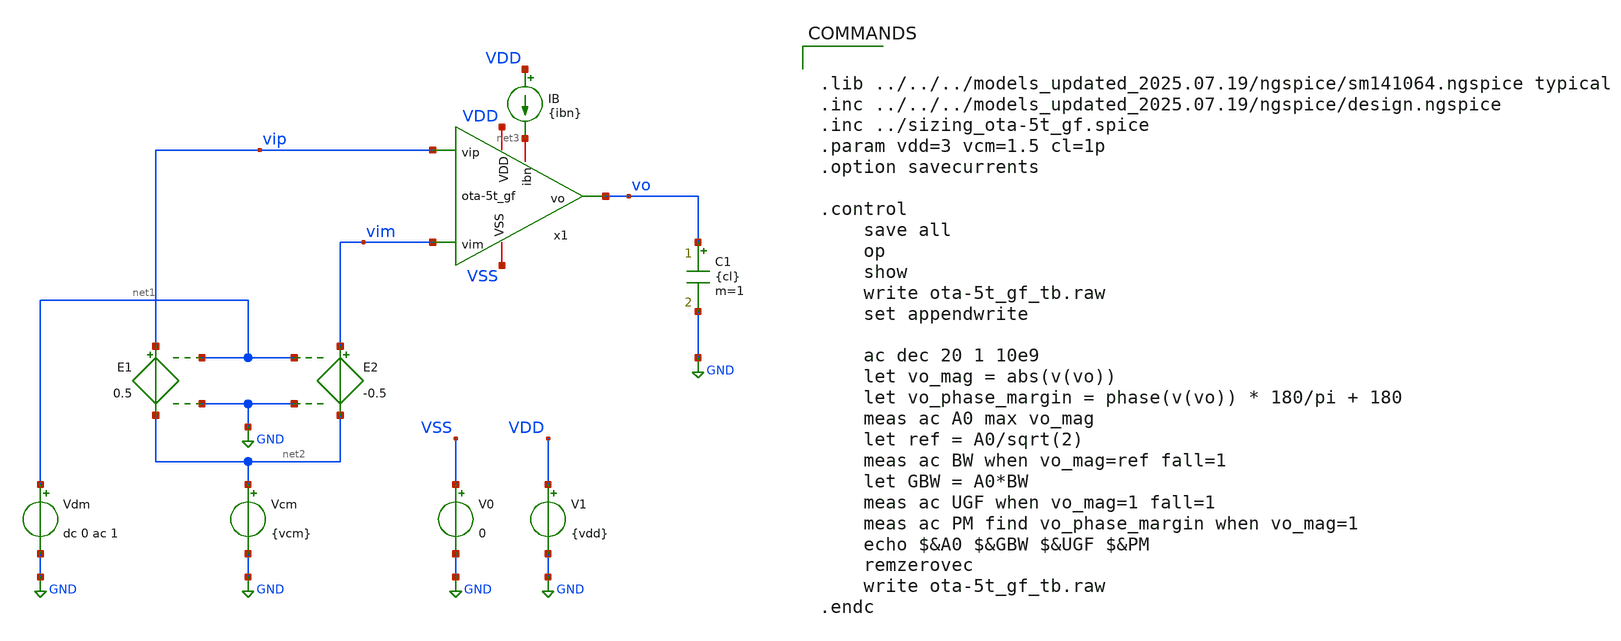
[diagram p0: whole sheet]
** sch_path: designs/libs/bmurmann_gmoverid/ota-5t/xschem/ota-5t_gf_tb.sch
**.subckt ota-5t_gf_tb
x1 vip vim vo VDD VSS net3 ota-5t_gf
E1 vip net2 net1 GND 0.5
E2 vim net2 net1 GND -0.5
Vdm net1 GND dc 0 ac 1
Vcm net2 GND {vcm}
V0 VSS GND 0
V1 VDD GND {vdd}
C1 vo GND {cl} m=1
IB VDD net3 {ibn}
**** begin user architecture code


.lib ../../../models_updated_2025.07.19/ngspice/sm141064.ngspice typical
.inc ../../../models_updated_2025.07.19/ngspice/design.ngspice
.inc ../sizing_ota-5t_gf.spice
.param vdd=3 vcm=1.5 cl=1p
.option savecurrents

.control
    save all
    op
    show
    write ota-5t_gf_tb.raw
    set appendwrite

    ac dec 20 1 10e9
    let vo_mag = abs(v(vo))
    let vo_phase_margin = phase(v(vo)) * 180/pi + 180
    meas ac A0 max vo_mag
    let ref = A0/sqrt(2)
    meas ac BW when vo_mag=ref fall=1
    let GBW = A0*BW
    meas ac UGF when vo_mag=1 fall=1
    meas ac PM find vo_phase_margin when vo_mag=1
    echo $&A0 $&GBW $&UGF $&PM
    remzerovec
    write ota-5t_gf_tb.raw
.endc


**** end user architecture code
**.ends

* expanding   symbol:  ota-5t_gf.sym # of pins=6
** sym_path: ota-5t_gf.sym
** sch_path: ota-5t_gf.sch
.subckt ota-5t_gf vip vim vo VDD VSS ibn
*.ipin vip
*.ipin vim
*.opin vo
*.iopin VDD
*.iopin VSS
*.iopin ibn
XM2b vo vmirr VDD VDD pfet_03v3 L={L2} W={W2} nf={nf2} ad='int((nf+1)/2) * W/nf * 0.18u' as='int((nf+2)/2) * W/nf * 0.18u'
+ pd='2*int((nf+1)/2) * (W/nf + 0.18u)' ps='2*int((nf+2)/2) * (W/nf + 0.18u)' nrd='0.18u / W' nrs='0.18u / W'
+ sa=0 sb=0 sd=0 m=1
XM2a vmirr vmirr VDD VDD pfet_03v3 L={L2} W={W2} nf={nf2} ad='int((nf+1)/2) * W/nf * 0.18u' as='int((nf+2)/2) * W/nf * 0.18u'
+ pd='2*int((nf+1)/2) * (W/nf + 0.18u)' ps='2*int((nf+2)/2) * (W/nf + 0.18u)' nrd='0.18u / W' nrs='0.18u / W'
+ sa=0 sb=0 sd=0 m=1
XM1a vmirr vip vtail VSS nfet_03v3 L={L1} W={W1} nf={nf1} ad='int((nf+1)/2) * W/nf * 0.18u' as='int((nf+2)/2) * W/nf * 0.18u'
+ pd='2*int((nf+1)/2) * (W/nf + 0.18u)' ps='2*int((nf+2)/2) * (W/nf + 0.18u)' nrd='0.18u / W' nrs='0.18u / W'
+ sa=0 sb=0 sd=0 m=1
XM0b vtail ibn VSS VSS nfet_03v3 L={L0} W={W0} nf={nf0} ad='int((nf+1)/2) * W/nf * 0.18u' as='int((nf+2)/2) * W/nf * 0.18u'
+ pd='2*int((nf+1)/2) * (W/nf + 0.18u)' ps='2*int((nf+2)/2) * (W/nf + 0.18u)' nrd='0.18u / W' nrs='0.18u / W'
+ sa=0 sb=0 sd=0 m=1
XM1b vo vim vtail VSS nfet_03v3 L={L1} W={W1} nf={nf1} ad='int((nf+1)/2) * W/nf * 0.18u' as='int((nf+2)/2) * W/nf * 0.18u'
+ pd='2*int((nf+1)/2) * (W/nf + 0.18u)' ps='2*int((nf+2)/2) * (W/nf + 0.18u)' nrd='0.18u / W' nrs='0.18u / W'
+ sa=0 sb=0 sd=0 m=1
XM0a ibn ibn VSS VSS nfet_03v3 L={L0} W={W0} nf={nf0} ad='int((nf+1)/2) * W/nf * 0.18u' as='int((nf+2)/2) * W/nf * 0.18u'
+ pd='2*int((nf+1)/2) * (W/nf + 0.18u)' ps='2*int((nf+2)/2) * (W/nf + 0.18u)' nrd='0.18u / W' nrs='0.18u / W'
+ sa=0 sb=0 sd=0 m=1
.ends

.GLOBAL GND
.end
